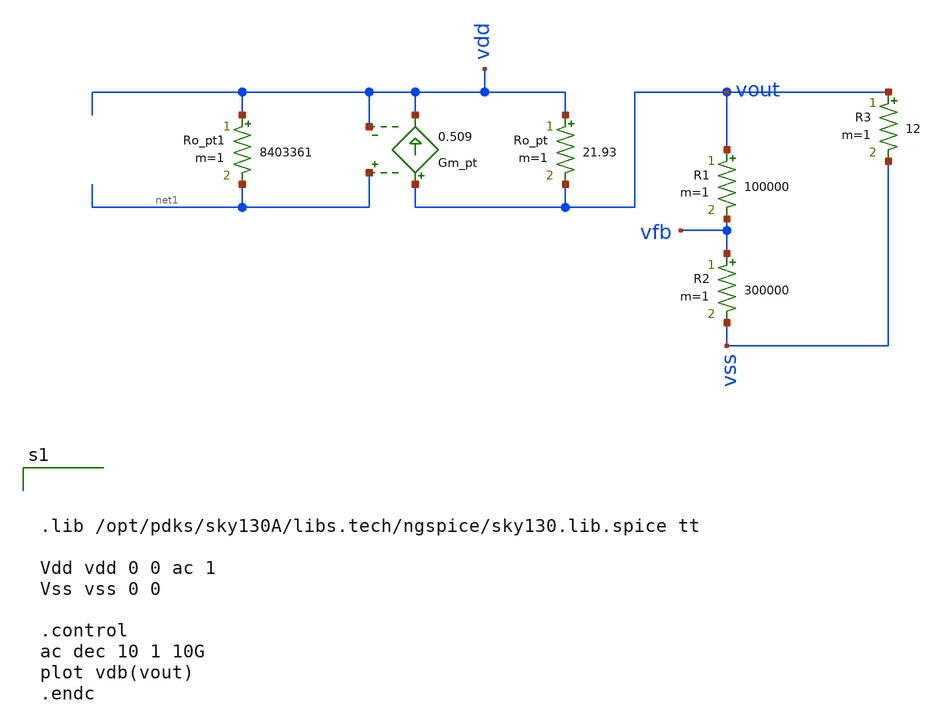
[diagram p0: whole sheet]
** sch_path: test/sstadex/untitled-1.sch
**.subckt untitled-1
Ro_pt vdd vout 21.93 m=1
Gm_pt vout vdd net1 vdd 0.509
R1 vout vfb 100000 m=1
R2 vfb vss 300000 m=1
Ro_pt1 vdd net1 8403361 m=1
R3 vout vss 12 m=1
**** begin user architecture code



.lib /opt/pdks/sky130A/libs.tech/ngspice/sky130.lib.spice tt

Vdd vdd 0 0 ac 1
Vss vss 0 0

.control
ac dec 10 1 10G
plot vdb(vout)
.endc



**** end user architecture code
**.ends
.end
